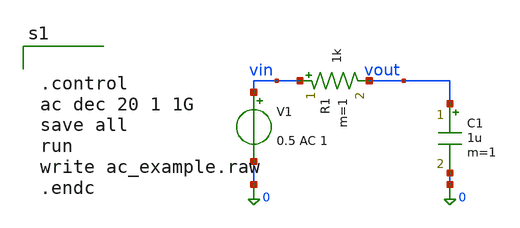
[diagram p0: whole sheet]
** sch_path: mag/ac_example.sch
**.subckt ac_example
V1 vin 0 0.5 AC 1
R1 vin vout 1k m=1
C1 vout 0 1u m=1
**** begin user architecture code


.control
ac dec 20 1 1G
save all
run
write ac_example.raw
.endc

**** end user architecture code
**.ends
.end
